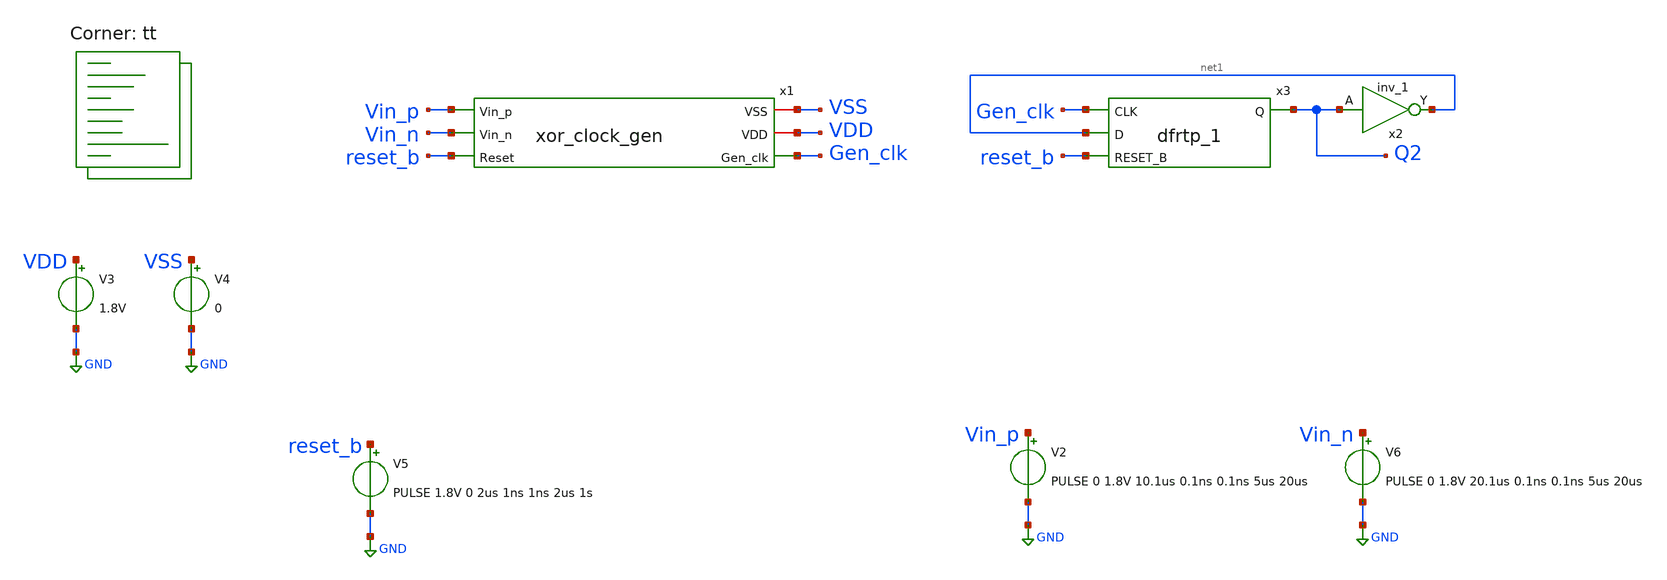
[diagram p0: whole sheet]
** sch_path: xschem/tests/xor_clock_gen/xor_clock_gen_test.sch
**.subckt xor_clock_gen_test
V3 VDD GND 1.8V
V4 VSS GND 0
x1 VSS Vin_p VDD Vin_n Gen_clk reset_b xor_clock_gen
V5 reset_b GND PULSE 1.8V 0 2us 1ns 1ns 2us 1s
V2 Vin_p GND PULSE 0 1.8V 10.1us 0.1ns 0.1ns 5us 20us
V6 Vin_n GND PULSE 0 1.8V 20.1us 0.1ns 0.1ns 5us 20us
x3 Gen_clk net1 reset_b VSS VSS VDD VDD Q2 sky130_fd_sc_hd__dfrtp_1
x2 Q2 VSS VSS VDD VDD net1 sky130_fd_sc_hd__inv_1
**** begin user architecture code
 *.lib $::SKYWATER_MODELS/sky130.lib.spice tt
.include $::SKYWATER_STDCELLS/sky130_fd_sc_hd.spice


.options acct list
.temp 25
*vvcc VDD 0 dc 1.8
*vvss VSS 0 0
.control
tran 0.01u 80u
*plot RST_PLS clk+2 Pulse+4
plot Vin_p-Vin_n reset_b-2 Gen_clk Q2+2
write xor_clock_gen_test.raw
.endc


.lib $::SKYWATER_MODELS/sky130.lib.spice tt
**** end user architecture code
**.ends

* expanding   symbol:  src/xor_clock_gen/xor_clock_gen.sym # of pins=6
** sym_path: xschem/src/xor_clock_gen/xor_clock_gen.sym
** sch_path: xschem/src/xor_clock_gen/xor_clock_gen.sch
.subckt xor_clock_gen VSS Vin_p VDD Vin_n Gen_clk Reset
*.ipin Vin_p
*.iopin VSS
*.opin Gen_clk
*.iopin VDD
*.ipin Vin_n
*.ipin Reset
x2 Vin_p Vin_n VSS VSS VDD VDD net1 sky130_fd_sc_hd__xor2_1
x3 net1 VSS VSS VDD VDD net9 sky130_fd_sc_hd__clkdlybuf4s50_1
x4 net21 VSS VSS VDD VDD net22 sky130_fd_sc_hd__clkdlybuf4s50_1
x5 net22 VSS VSS VDD VDD net2 sky130_fd_sc_hd__clkdlybuf4s50_1
x6 net2 VSS VSS VDD VDD net3 sky130_fd_sc_hd__clkdlybuf4s50_1
x7 net3 VSS VSS VDD VDD net4 sky130_fd_sc_hd__clkdlybuf4s50_1
x8 net4 VSS VSS VDD VDD net8 sky130_fd_sc_hd__clkdlybuf4s50_1
x13 net8 VSS VSS VDD VDD net6 sky130_fd_sc_hd__clkdlybuf4s50_1
x15 net6 VSS VSS VDD VDD net7 sky130_fd_sc_hd__clkdlybuf4s50_1
x16 net7 VSS VSS VDD VDD net5 sky130_fd_sc_hd__clkdlybuf4s50_1
x17 net9 VSS VSS VDD VDD net10 sky130_fd_sc_hd__clkdlybuf4s50_1
x18 net10 VSS VSS VDD VDD net11 sky130_fd_sc_hd__clkdlybuf4s50_1
x20 net11 VSS VSS VDD VDD net12 sky130_fd_sc_hd__clkdlybuf4s50_1
x21 net12 VSS VSS VDD VDD net13 sky130_fd_sc_hd__clkdlybuf4s50_1
x22 net13 VSS VSS VDD VDD net16 sky130_fd_sc_hd__clkdlybuf4s50_1
x23 net16 VSS VSS VDD VDD net14 sky130_fd_sc_hd__clkdlybuf4s50_1
x24 net14 VSS VSS VDD VDD net15 sky130_fd_sc_hd__clkdlybuf4s50_1
x25 net15 VSS VSS VDD VDD net21 sky130_fd_sc_hd__clkdlybuf4s50_1
x9 net5 VSS VSS VDD VDD net17 sky130_fd_sc_hd__clkbuf_1
x14 net17 VSS VSS VDD VDD net18 sky130_fd_sc_hd__clkbuf_2
x19 net18 VSS VSS VDD VDD net19 sky130_fd_sc_hd__clkbuf_4
x26 net19 VSS VSS VDD VDD net20 sky130_fd_sc_hd__clkbuf_8
x27 net20 VSS VSS VDD VDD Gen_clk sky130_fd_sc_hd__clkbuf_16
XC2 net17 VSS sky130_fd_pr__cap_mim_m3_1 W=10 L=10 MF=1 m=1
.ends

.GLOBAL GND
.end
